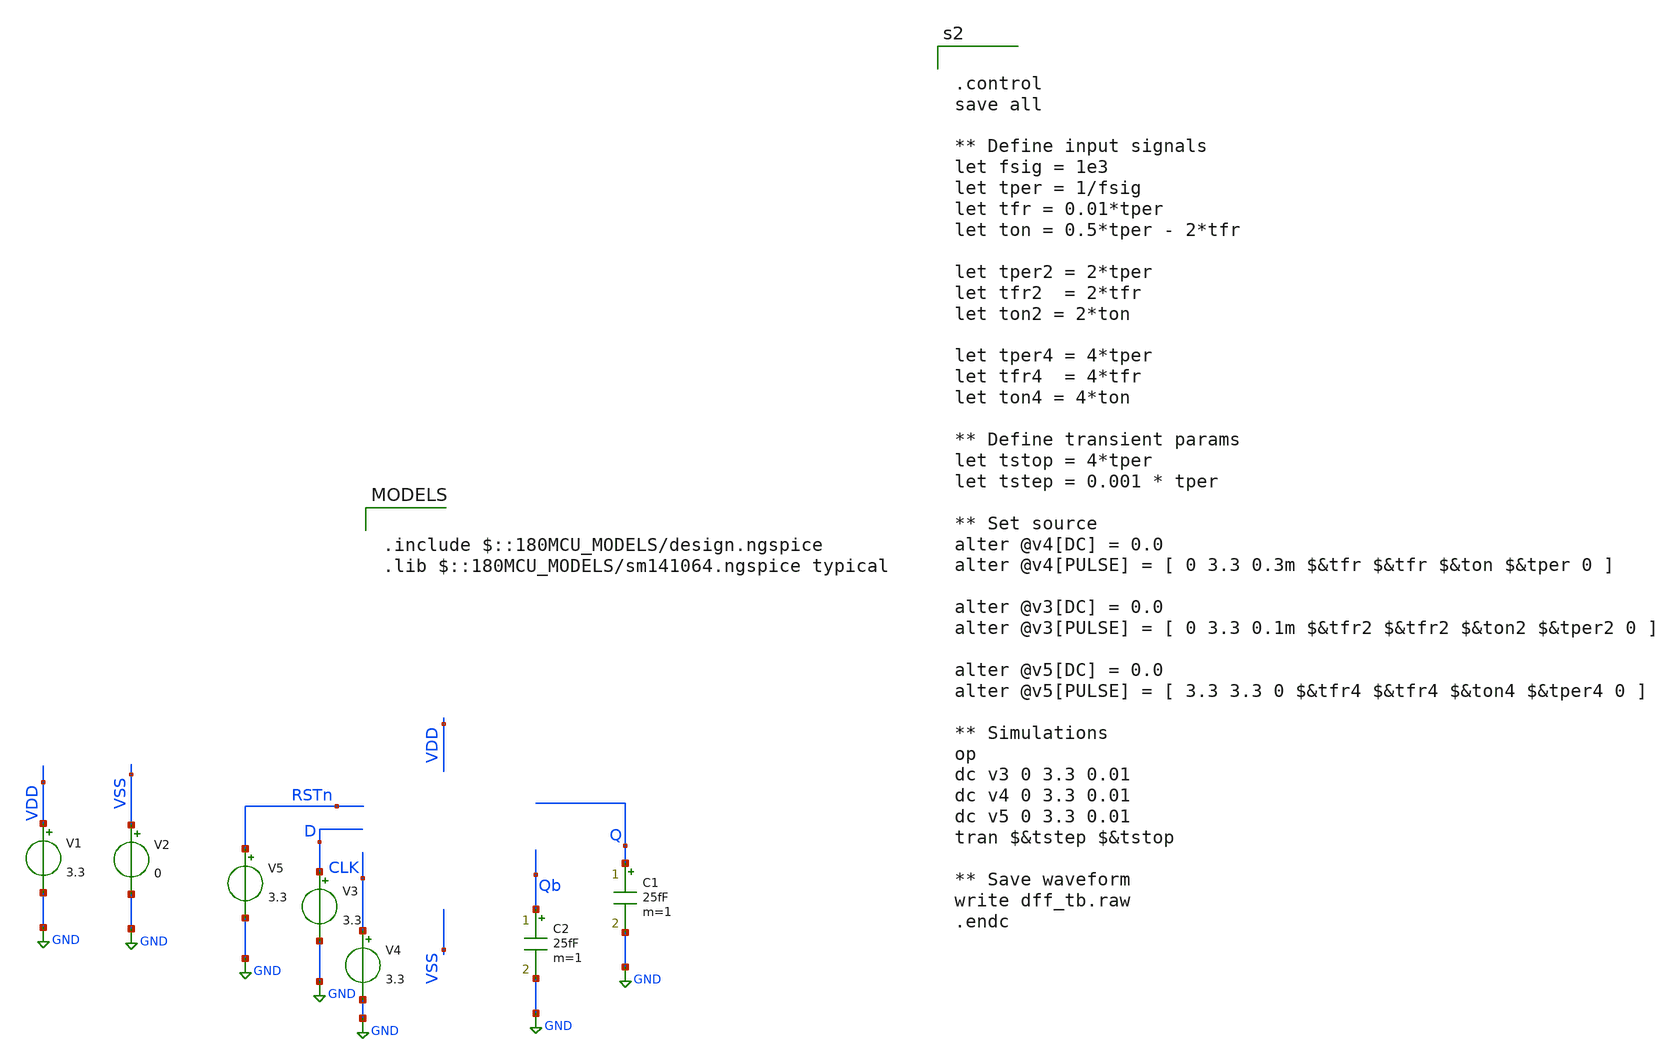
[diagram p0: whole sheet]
** sch_path: dff_postpex_tb.sch
**.subckt dff_postpex_tb
V1 VDD GND 3.3
V2 VSS GND 0
V3 D GND 3.3
C1 Q GND 25fF m=1
V4 CLK GND 3.3
C2 Qb GND 25fF m=1
V5 RSTn GND 3.3
**** begin user architecture code

.include $::180MCU_MODELS/design.ngspice
.lib $::180MCU_MODELS/sm141064.ngspice typical



.subckt dff_flat VDD CLK RSTN VSS D Q Qb
X0 a_n249_n4912# a_n1374_n6642# RSTN.t1 VSS.t9 nfet_03v3 ad=0.2646p pd=2.1u as=0.2646p ps=2.1u
+ w=0.42u l=0.28u
X1 VSS.t25 a_n359_n5759.t3 Q.t0 VSS.t24 nfet_03v3 ad=0.2646p pd=2.1u as=0.2646p ps=2.1u w=0.42u
+ l=0.28u
X2 a_n359_n5759.t1 a_n249_n4912# VDD.t14 VDD.t13 pfet_03v3 ad=0.1092p pd=0.94u as=0.2822p ps=2.18u
+ w=0.42u l=0.28u
X3 VDD.t25 a_n89_n4912# a_881_n5758# VDD.t24 pfet_03v3 ad=0.2822p pd=2.18u as=0.1092p ps=0.94u
+ w=0.42u l=0.28u
X4 VDD.t9 a_n1374_n6642# a_1067_n6116# VDD.t8 pfet_03v3 ad=0.2822p pd=2.18u as=0.1092p ps=0.94u
+ w=0.42u l=0.28u
X5 a_2281_n4424# D.t0 a_1056_n4015# VSS.t12 nfet_03v3 ad=0.1092p pd=0.94u as=0.2646p ps=2.1u w=0.42u
+ l=0.28u
X6 VSS.t11 CLK.t0 a_n1342_n5730# VSS.t10 nfet_03v3 ad=0.2646p pd=2.1u as=0.2646p ps=2.1u w=0.42u
+ l=0.28u
X7 a_2280_n3998# D.t1 a_1056_n4015# VDD.t12 pfet_03v3 ad=0.1092p pd=0.94u as=0.2822p ps=2.18u
+ w=0.42u l=0.28u
X8 VDD.t11 CLK.t1 a_n1342_n5730# VDD.t10 pfet_03v3 ad=0.2822p pd=2.18u as=0.2822p ps=2.18u w=0.42u
+ l=0.28u
X9 VSS.t7 a_n1342_n5730# a_n1374_n6642# VSS.t6 nfet_03v3 ad=0.2667p pd=2.11u as=0.2625p ps=2.09u
+ w=0.42u l=0.28u
X10 a_1059_n5756# RSTN.t4 a_881_n5758# VSS.t20 nfet_03v3 ad=0.1092p pd=0.94u as=0.2646p ps=2.1u
+ w=0.42u l=0.28u
X11 VSS.t15 a_1056_n4015# RSTN.t3 VSS.t14 nfet_03v3 ad=0.2646p pd=2.1u as=0.2646p ps=2.1u w=0.42u
+ l=0.28u
X12 VSS.t5 a_n1342_n5730# a_1068_n6542# VSS.t4 nfet_03v3 ad=0.2646p pd=2.1u as=0.1092p ps=0.94u
+ w=0.42u l=0.28u
X13 VSS.t1 a_n912_n3722# Qb.t1 VSS.t0 nfet_03v3 ad=0.2646p pd=2.1u as=0.2646p ps=2.1u w=0.42u
+ l=0.28u
X14 VSS.t19 a_n89_n4912# a_n181_n5757# VSS.t18 nfet_03v3 ad=0.2646p pd=2.1u as=0.1092p ps=0.94u
+ w=0.42u l=0.28u
X15 VDD.t19 a_n359_n5759.t4 Q.t1 VDD.t18 pfet_03v3 ad=0.2822p pd=2.18u as=0.2822p ps=2.18u w=0.42u
+ l=0.28u
X16 a_n249_n4912# a_n1342_n5730# RSTN.t0 VDD.t5 pfet_03v3 ad=0.2822p pd=2.18u as=0.2822p ps=2.18u
+ w=0.42u l=0.28u
X17 VSS.t22 a_n359_n5759.t5 a_n912_n3722# VSS.t21 nfet_03v3 ad=0.2646p pd=2.1u as=0.2646p ps=2.1u
+ w=0.42u l=0.28u
X18 VDD.t4 a_n1342_n5730# a_n1374_n6642# VDD.t3 pfet_03v3 ad=0.2822p pd=2.18u as=0.2822p ps=2.18u
+ w=0.42u l=0.28u
X19 a_881_n5758# a_n1374_n6642# a_1056_n4015# VSS.t8 nfet_03v3 ad=0.2646p pd=2.1u as=0.2646p ps=2.1u
+ w=0.42u l=0.28u
X20 VDD.t1 a_n912_n3722# Qb.t0 VDD.t0 pfet_03v3 ad=0.2822p pd=2.18u as=0.2822p ps=2.18u w=0.42u
+ l=0.28u
X21 VSS.t3 a_n1342_n5730# a_2281_n4424# VSS.t2 nfet_03v3 ad=0.2646p pd=2.1u as=0.1092p ps=0.94u
+ w=0.42u l=0.28u
X22 VDD.t23 a_n89_n4912# a_n359_n5759.t2 VDD.t22 pfet_03v3 ad=0.2822p pd=2.18u as=0.1092p ps=0.94u
+ w=0.42u l=0.28u
X23 VDD.t7 a_n1374_n6642# a_2280_n3998# VDD.t6 pfet_03v3 ad=0.2822p pd=2.18u as=0.1092p ps=0.94u
+ w=0.42u l=0.28u
X24 a_1067_n6116# a_n359_n5759.t6 a_n249_n4912# VDD.t17 pfet_03v3 ad=0.1092p pd=0.94u as=0.2822p
+ ps=2.18u w=0.42u l=0.28u
X25 a_881_n5758# RSTN.t5 VDD.t27 VDD.t26 pfet_03v3 ad=0.1092p pd=0.94u as=0.2822p ps=2.18u w=0.42u
+ l=0.28u
X26 VSS.t17 a_n89_n4912# a_1059_n5756# VSS.t16 nfet_03v3 ad=0.2646p pd=2.1u as=0.1092p ps=0.94u
+ w=0.42u l=0.28u
X27 VDD.t21 a_1056_n4015# RSTN.t2 VDD.t20 pfet_03v3 ad=0.2822p pd=2.18u as=0.2822p ps=2.18u w=0.42u
+ l=0.28u
X28 a_881_n5758# a_n1342_n5730# a_1056_n4015# VDD.t2 pfet_03v3 ad=0.2822p pd=2.18u as=0.2822p
+ ps=2.18u w=0.42u l=0.28u
X29 a_1068_n6542# a_n359_n5759.t7 a_n249_n4912# VSS.t23 nfet_03v3 ad=0.1092p pd=0.94u as=0.2646p
+ ps=2.1u w=0.42u l=0.28u
X30 a_n181_n5757# a_n249_n4912# a_n359_n5759.t0 VSS.t13 nfet_03v3 ad=0.1092p pd=0.94u as=0.2646p
+ ps=2.1u w=0.42u l=0.28u
X31 VDD.t16 a_n359_n5759.t8 a_n912_n3722# VDD.t15 pfet_03v3 ad=0.2822p pd=2.18u as=0.2822p ps=2.18u
+ w=0.42u l=0.28u
R0 RSTN.t5 RSTN.n3 72.3487
R1 RSTN RSTN.t5 24.9493
R2 RSTN.n3 RSTN.t4 16.9469
R3 RSTN.n1 RSTN.t1 12.9962
R4 RSTN.n0 RSTN.t2 12.66
R5 RSTN.n0 RSTN.t3 12.3135
R6 RSTN.n1 RSTN.t0 12.0263
R7 RSTN.n3 RSTN.n2 9.90023
R8 RSTN.n2 RSTN.n1 0.39464
R9 RSTN.n2 RSTN.n0 0.156576
R10 VSS.n23 VSS.n16 749278
R11 VSS.n16 VSS.t12 91327.6
R12 VSS.n5 VSS.n3 64653.5
R13 VSS.n50 VSS.n3 47027.8
R14 VSS.n13 VSS.n8 11150.5
R15 VSS.t0 VSS.n46 10656.3
R16 VSS.n46 VSS.n45 9310.54
R17 VSS.n6 VSS.n3 9172.39
R18 VSS.n17 VSS.n8 8859.18
R19 VSS.n46 VSS.n7 7710.44
R20 VSS.n43 VSS.n9 6769.51
R21 VSS.n35 VSS.n34 6625.47
R22 VSS.n45 VSS.n8 5874.35
R23 VSS.t6 VSS.n49 4464.13
R24 VSS.n13 VSS.n11 4354.26
R25 VSS.n30 VSS.n10 4226.8
R26 VSS.n29 VSS.n11 4102.23
R27 VSS.n45 VSS.n44 3676.98
R28 VSS.n24 VSS.n23 3564.92
R29 VSS.n44 VSS.t8 2894.81
R30 VSS.n47 VSS.n7 2588.74
R31 VSS.t24 VSS.n3 2474.65
R32 VSS.n49 VSS.n48 2224.45
R33 VSS.n49 VSS.t10 1774.36
R34 VSS.n48 VSS.n6 1755.92
R35 VSS.n22 VSS.n21 1702.15
R36 VSS.t14 VSS.n24 1689.9
R37 VSS.n24 VSS.n10 1589.78
R38 VSS.t10 VSS.n5 1493.57
R39 VSS.t2 VSS.n15 1430.46
R40 VSS.n25 VSS.t14 1413.04
R41 VSS.t20 VSS.n9 1360.03
R42 VSS.n21 VSS.t8 1205.49
R43 VSS.t21 VSS.n7 1196.19
R44 VSS.n48 VSS.n47 1177.13
R45 VSS.n18 VSS.t16 1172.44
R46 VSS.n23 VSS.n22 1095.11
R47 VSS.n25 VSS.n11 1090.87
R48 VSS.n36 VSS.t18 1070.49
R49 VSS.n34 VSS.t23 1055.67
R50 VSS.n42 VSS.t21 992.063
R51 VSS.n30 VSS.t9 940.115
R52 VSS.n50 VSS.t6 920.712
R53 VSS.t12 VSS.t2 915.494
R54 VSS.n18 VSS.n10 900.433
R55 VSS.n34 VSS.n33 836.077
R56 VSS.n36 VSS.n35 822.135
R57 VSS.n32 VSS.n30 797.649
R58 VSS.t16 VSS.t20 750.361
R59 VSS.t18 VSS.t13 685.112
R60 VSS.n17 VSS.n16 674.74
R61 VSS.n38 VSS.n7 671.655
R62 VSS.n43 VSS.n42 615.08
R63 VSS.n33 VSS.t24 604.99
R64 VSS.t4 VSS.n32 576.241
R65 VSS.t9 VSS.n29 492.724
R66 VSS.n44 VSS.n43 472.2
R67 VSS.n15 VSS.n13 469.19
R68 VSS.t13 VSS.n6 466.733
R69 VSS.n47 VSS.t0 415.238
R70 VSS.t23 VSS.t4 368.795
R71 VSS.n35 VSS.n9 317.529
R72 VSS.n22 VSS.n17 57.864
R73 VSS.n21 VSS.n20 15.3475
R74 VSS.n51 VSS.t7 12.5437
R75 VSS.n37 VSS.t19 12.4687
R76 VSS.n31 VSS.t5 12.4687
R77 VSS.n19 VSS.t17 12.4687
R78 VSS.n26 VSS.t15 12.4687
R79 VSS.n41 VSS.t22 12.4687
R80 VSS.n4 VSS.t11 12.4687
R81 VSS.n1 VSS.t25 12.4687
R82 VSS.n38 VSS.t1 12.4687
R83 VSS.n14 VSS.t3 12.4675
R84 VSS.n29 VSS.n28 11.6695
R85 VSS.n15 VSS.n14 10.4017
R86 VSS.n19 VSS.n18 10.4005
R87 VSS.n26 VSS.n25 10.4005
R88 VSS.n5 VSS.n4 10.4005
R89 VSS.n33 VSS.n1 10.4005
R90 VSS.n51 VSS.n50 10.4005
R91 VSS.n42 VSS.n41 10.4005
R92 VSS.n32 VSS.n31 10.4005
R93 VSS.n37 VSS.n36 10.4005
R94 VSS.n31 VSS.n0 9.86036
R95 VSS.n28 VSS.n27 6.42418
R96 VSS.n20 VSS.n19 6.02652
R97 VSS.n39 VSS.n38 5.75457
R98 VSS.n39 VSS.n2 5.48837
R99 VSS.n41 VSS.n40 5.44665
R100 VSS.n40 VSS.n37 5.3877
R101 VSS.n27 VSS.n26 4.66984
R102 VSS.n14 VSS.n12 4.6547
R103 VSS.n20 VSS.n12 1.34731
R104 VSS.n40 VSS.n39 1.2245
R105 VSS.n27 VSS.n12 1.03428
R106 VSS.n52 VSS.n2 0.820259
R107 VSS VSS.n0 0.783577
R108 VSS.n28 VSS.n0 0.664346
R109 VSS.n53 VSS.n52 0.652808
R110 VSS VSS.n53 0.348192
R111 VSS.n4 VSS.n2 0.323682
R112 VSS.n53 VSS.n1 0.322765
R113 VSS.n52 VSS.n51 0.314599
R114 a_n359_n5759.t8 a_n359_n5759.t5 69.3505
R115 a_n359_n5759.t4 a_n359_n5759.t3 69.3505
R116 a_n359_n5759.t6 a_n359_n5759.t7 53.4469
R117 a_n359_n5759.n2 a_n359_n5759.t6 35.2609
R118 a_n359_n5759.n1 a_n359_n5759.t8 30.3133
R119 a_n359_n5759.n2 a_n359_n5759.t4 25.048
R120 a_n359_n5759.t0 a_n359_n5759.n3 12.3005
R121 a_n359_n5759.n1 a_n359_n5759.n0 5.78668
R122 a_n359_n5759.n0 a_n359_n5759.t2 4.33383
R123 a_n359_n5759.n0 a_n359_n5759.t1 4.33383
R124 a_n359_n5759.n3 a_n359_n5759.n2 0.519935
R125 a_n359_n5759.n3 a_n359_n5759.n1 0.494983
R126 Q Q.t0 12.6202
R127 Q Q.t1 12.341
R128 VDD.n8 VDD.t5 715.11
R129 VDD.n11 VDD.t2 714.49
R130 VDD.n18 VDD.t3 713.694
R131 VDD.n14 VDD.t0 713.688
R132 VDD.n17 VDD.t10 713.688
R133 VDD.n12 VDD.t22 713.688
R134 VDD.n16 VDD.t15 713.688
R135 VDD.n9 VDD.t6 713.688
R136 VDD.n6 VDD.t20 713.688
R137 VDD.n0 VDD.t24 713.688
R138 VDD.n3 VDD.t8 713.688
R139 VDD.n2 VDD.t18 713.688
R140 VDD.t22 VDD.t13 434.784
R141 VDD.t6 VDD.t12 434.784
R142 VDD.t24 VDD.t26 434.784
R143 VDD.t8 VDD.t17 434.784
R144 VDD.n0 VDD.t27 13.7623
R145 VDD.n13 VDD.t14 12.5331
R146 VDD.n17 VDD.t11 12.1992
R147 VDD.n16 VDD.t16 12.1992
R148 VDD.n6 VDD.t21 12.1992
R149 VDD.n3 VDD.t9 12.1992
R150 VDD.n2 VDD.t19 12.1992
R151 VDD.n14 VDD.t1 12.198
R152 VDD.n10 VDD.t7 12.1968
R153 VDD.n18 VDD.t4 12.192
R154 VDD.n12 VDD.t23 12.1422
R155 VDD.n1 VDD.t25 12.1411
R156 VDD.n19 VDD.n18 11.4596
R157 VDD.n16 VDD.n15 9.90617
R158 VDD.n4 VDD.n2 7.0573
R159 VDD.n7 VDD.n5 5.46986
R160 VDD.n5 VDD.n1 5.05424
R161 VDD.n4 VDD.n3 5.0066
R162 VDD.n20 VDD.n19 3.429
R163 VDD.n11 VDD.n10 1.6793
R164 VDD.n19 VDD.n17 1.5236
R165 VDD.n9 VDD.n8 1.27962
R166 VDD.n13 VDD.n12 1.1387
R167 VDD VDD.n11 0.864995
R168 VDD.n5 VDD.n4 0.845079
R169 VDD.n20 VDD.n16 0.527474
R170 VDD.n15 VDD.n14 0.516611
R171 VDD.n15 VDD.n13 0.457423
R172 VDD.n8 VDD.n7 0.351026
R173 VDD VDD.n20 0.00545413
R174 VDD.n10 VDD.n9 0.00286842
R175 VDD.n7 VDD.n6 0.00168421
R176 VDD.n1 VDD.n0 0.00153448
R177 D.t1 D.t0 53.4469
R178 D D.t1 24.9505
R179 CLK.t1 CLK.t0 69.3505
R180 CLK CLK.t1 24.9517
R181 Qb Qb.t1 12.6395
R182 Qb Qb.t0 12.3217
C0 a_n1374_n6642# a_1056_n4015# 0.2678f
C1 RSTN a_1056_n4015# 0.10365f
C2 a_n249_n4912# a_n1374_n6642# 0.23084f
C3 a_n249_n4912# RSTN 0.11019f
C4 a_n1374_n6642# RSTN 0.22275f
C5 a_881_n5758# a_n1342_n5730# 0.31376f
C6 a_881_n5758# VDD 1.18904f
C7 VDD a_n912_n3722# 0.83176f
C8 VDD a_n89_n4912# 0.80322f
C9 VDD a_n1342_n5730# 1.71536f
C10 a_881_n5758# a_1056_n4015# 0.25267f
C11 a_881_n5758# a_n249_n4912# 0.19693f
C12 D VDD 0.18707f
C13 a_881_n5758# a_n1374_n6642# 0.24946f
C14 a_881_n5758# RSTN 0.35092f
C15 a_n89_n4912# a_n249_n4912# 0.28644f
C16 a_n89_n4912# RSTN 0.29193f
C17 VDD a_1056_n4015# 0.95856f
C18 a_n249_n4912# a_n1342_n5730# 0.21283f
C19 a_n1374_n6642# a_n1342_n5730# 1.67868f
C20 VDD a_n249_n4912# 0.56511f
C21 VDD a_n1374_n6642# 1.886f
C22 VDD RSTN 0.76938f
C23 VDD CLK 0.28794f
C24 VDD Qb 0.10704f
C25 Q VSS 0.25589f
C26 CLK VSS 0.39888f
C27 RSTN VSS 1.33038f
C28 D VSS 0.27844f
C29 Qb VSS 0.15428f
C30 VDD VSS 18.83505f
C31 a_n89_n4912# VSS 1.32962f
C32 a_n249_n4912# VSS 2.53842f
C33 a_881_n5758# VSS 0.89126f
C34 a_1056_n4015# VSS 1.26966f
C35 a_n1374_n6642# VSS 5.44569f
C36 a_n1342_n5730# VSS 6.88765f
C37 a_n912_n3722# VSS 0.62392f
C38 VDD.n8 VSS 0.11133f
C39 VDD.n11 VSS 0.13113f
C40 VDD.n19 VSS 0.21025f
C41 VDD.n20 VSS 0.10843f
C42 a_n359_n5759.t8 VSS 0.19196f
C43 a_n359_n5759.n1 VSS 1.35777f
C44 a_n359_n5759.t6 VSS 0.11284f
C45 a_n359_n5759.n2 VSS 0.45569f
C46 a_n359_n5759.n3 VSS 0.14466f
.ends

X0 VDD CLK RSTN VSS D Q Qb dff_flat




.control
save all

** Define input signals
let fsig = 1e3
let tper = 1/fsig
let tfr = 0.01*tper
let ton = 0.5*tper - 2*tfr

let tper2 = 2*tper
let tfr2  = 2*tfr
let ton2 = 2*ton

let tper4 = 4*tper
let tfr4  = 4*tfr
let ton4 = 4*ton

** Define transient params
let tstop = 4*tper
let tstep = 0.001 * tper

** Set source
alter @v4[DC] = 0.0
alter @v4[PULSE] = [ 0 3.3 0.3m $&tfr $&tfr $&ton $&tper 0 ]

alter @v3[DC] = 0.0
alter @v3[PULSE] = [ 0 3.3 0.1m $&tfr2 $&tfr2 $&ton2 $&tper2 0 ]

alter @v5[DC] = 0.0
alter @v5[PULSE] = [ 3.3 3.3 0 $&tfr4 $&tfr4 $&ton4 $&tper4 0 ]

** Simulations
op
dc v3 0 3.3 0.01
dc v4 0 3.3 0.01
dc v5 0 3.3 0.01
tran $&tstep $&tstop

** Save waveform
write dff_tb.raw
.endc


**** end user architecture code
**.ends
.GLOBAL GND
.end
